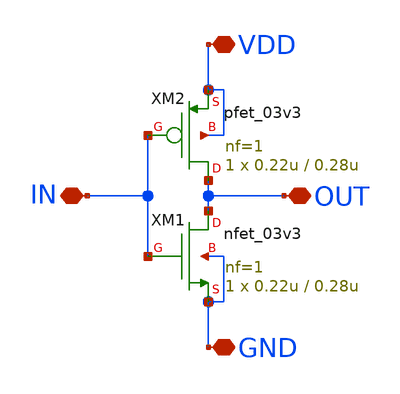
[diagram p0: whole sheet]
** sch_path: gf_tutorials/inverter/inverter.sch
**.subckt inverter GND VDD OUT IN
*.iopin GND
*.iopin VDD
*.iopin OUT
*.iopin IN
XM1 OUT IN GND GND nfet_03v3 L=0.28u W=0.22u nf=1 ad='int((nf+1)/2) * W/nf * 0.18u' as='int((nf+2)/2) * W/nf * 0.18u'
+ pd='2*int((nf+1)/2) * (W/nf + 0.18u)' ps='2*int((nf+2)/2) * (W/nf + 0.18u)' nrd='0.18u / W' nrs='0.18u / W'
+ sa=0 sb=0 sd=0 m=1
XM2 OUT IN VDD VDD pfet_03v3 L=0.28u W=0.22u nf=1 ad='int((nf+1)/2) * W/nf * 0.18u' as='int((nf+2)/2) * W/nf * 0.18u'
+ pd='2*int((nf+1)/2) * (W/nf + 0.18u)' ps='2*int((nf+2)/2) * (W/nf + 0.18u)' nrd='0.18u / W' nrs='0.18u / W'
+ sa=0 sb=0 sd=0 m=1
**.ends
.end
